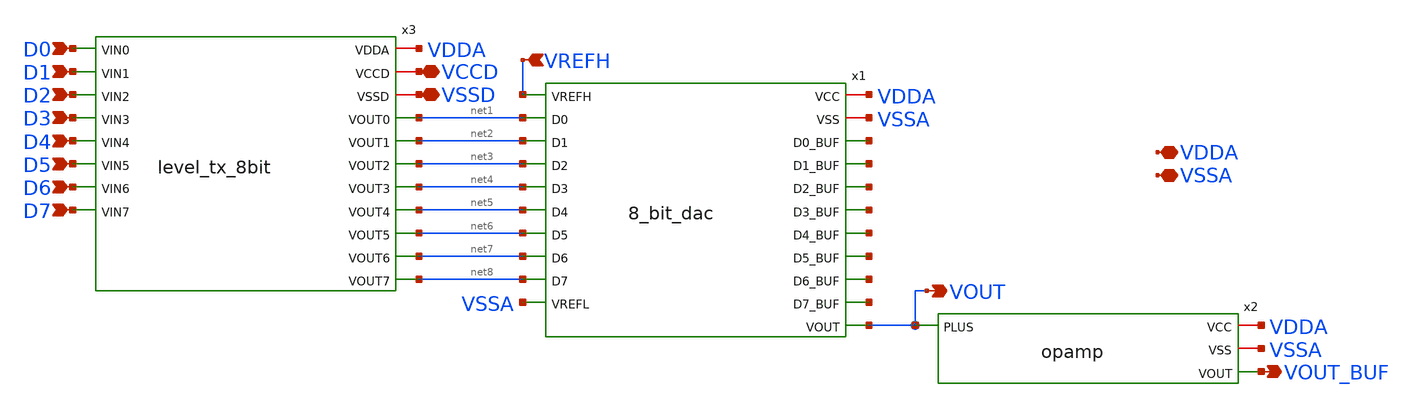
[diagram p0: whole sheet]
** sch_path: Layout_v2/Post-layout/lvs/z_stuff/All_schematic/8_bit_dac_tx_buffer.sch
**.subckt 8_bit_dac_tx_buffer VSSD VCCD VDDA VSSA VOUT_BUF D0 D1 D2 D3 D4 D5 D6 D7 VREFH VOUT
*.iopin VSSD
*.iopin VCCD
*.iopin VDDA
*.iopin VSSA
*.opin VOUT_BUF
*.ipin D0
*.ipin D1
*.ipin D2
*.ipin D3
*.ipin D4
*.ipin D5
*.ipin D6
*.ipin D7
*.ipin VREFH
*.opin VOUT
x1 VDDA VREFH VSSA net9 net10 net11 net12 net13 net14 net15 net8 net16 VOUT net1 net2 net3 net4 net5
+ net6 net7 VSSA 8_bit_dac
x2 VDDA VSSA VOUT VOUT_BUF opamp
x3 VSSD VCCD VDDA D0 D4 net5 net1 D1 D5 net6 net2 D2 D6 net3 net7 D7 D3 net8 net4 level_tx_8bit
**.ends
.end
